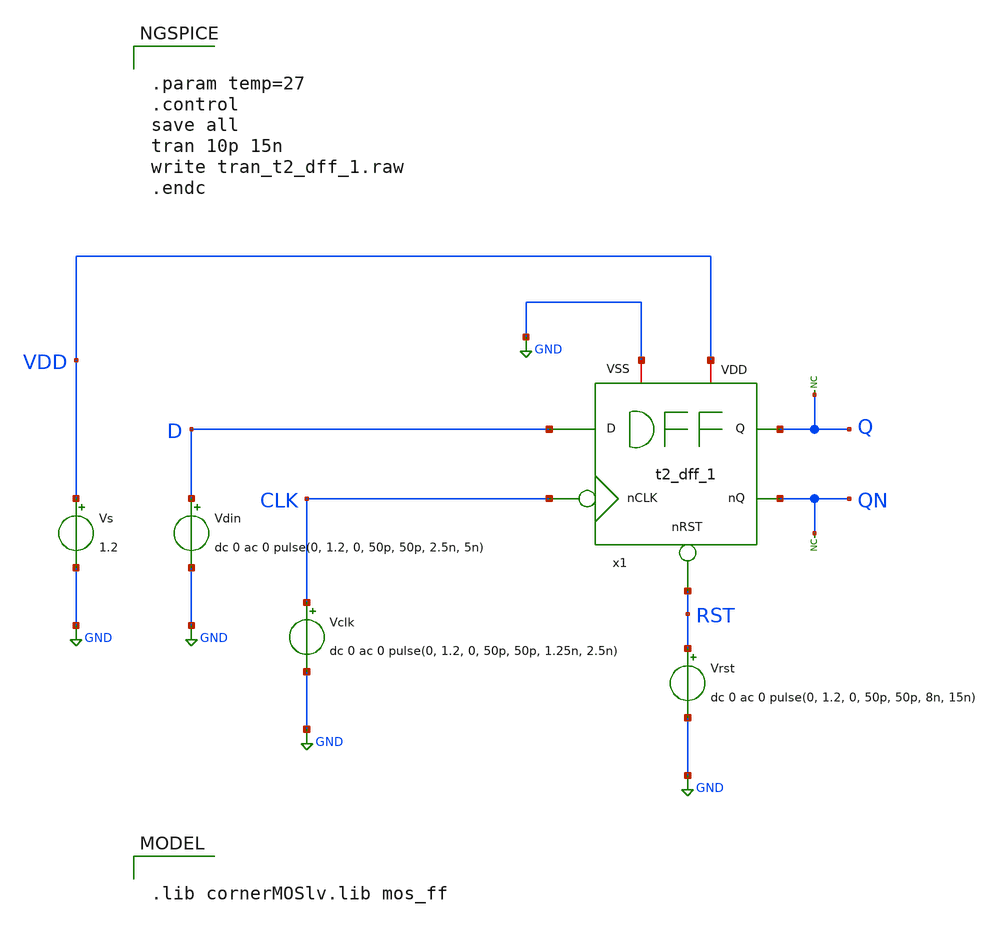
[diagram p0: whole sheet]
** sch_path: Team 2 Design/design_data/xschem/t2_dff_1_tb.sch
**.subckt t2_dff_1_tb
Vs VDD GND 1.2
* noconn Q
* noconn QN
Vdin D GND dc 0 ac 0 pulse(0, 1.2, 0, 50p, 50p, 2.5n, 5n)
Vclk CLK GND dc 0 ac 0 pulse(0, 1.2, 0, 50p, 50p, 1.25n, 2.5n)
Vrst RST GND dc 0 ac 0 pulse(0, 1.2, 0, 50p, 50p, 8n, 15n)
x1 VDD GND D CLK RST Q QN t2_dff_1
**** begin user architecture code


.param temp=27
.control
save all
tran 10p 15n
write tran_t2_dff_1.raw
.endc



.lib cornerMOSlv.lib mos_ff

**** end user architecture code
**.ends

* expanding   symbol:  t2_dff_1.sym # of pins=7
** sym_path: Team 2 Design/design_data/xschem/t2_dff_1.sym
** sch_path: Team 2 Design/design_data/xschem/t2_dff_1.sch
.subckt t2_dff_1 VDD VSS D CLK RST Q QN
*.iopin VSS
*.ipin D
*.ipin RST
*.opin Q
*.iopin VDD
*.opin QN
*.ipin CLK
x3 VDD net1 QN Q VSS t2_nand2
x4 VDD VSS Q net2 RST QN t2_nand3
x1 VDD VSS net4 net5 RST net1 t2_nand3
x2 VDD VSS net1 net5 net3 net2 t2_nand3
x6 VDD net3 net1 net4 VSS t2_nand2
x5 VDD VSS net2 D RST net3 t2_nand3
x7 VDD CLK net5 VSS t2_inverter
.ends


* expanding   symbol:  t2_nand2.sym # of pins=5
** sym_path: Team 2 Design/design_data/xschem/t2_nand2.sym
** sch_path: Team 2 Design/design_data/xschem/t2_nand2.sch
.subckt t2_nand2 VDD inA inB out VSS
*.iopin VSS
*.ipin inA
*.ipin inB
*.opin out
*.iopin VDD
XM1 out inA VDD VDD sg13_lv_pmos w=1u l=0.45u ng=1 m=1 mm_ok=1
XM2 out inB VDD VDD sg13_lv_pmos w=1u l=0.45u ng=1 m=1 mm_ok=1
XM3 out inB net1 VSS sg13_lv_nmos w=0.5u l=0.45u ng=1 m=1 mm_ok=1
XM4 net1 inA VSS VSS sg13_lv_nmos w=0.5u l=0.45u ng=1 m=1 mm_ok=1
.ends


* expanding   symbol:  t2_nand3.sym # of pins=6
** sym_path: Team 2 Design/design_data/xschem/t2_nand3.sym
** sch_path: Team 2 Design/design_data/xschem/t2_nand3.sch
.subckt t2_nand3 VDD VSS inA inB inC out
*.iopin VSS
*.ipin inA
*.ipin inC
*.opin out
*.iopin VDD
*.ipin inB
XM1 out inB VDD VDD sg13_lv_pmos w=0.3u l=0.15u ng=1 m=1 mm_ok=1
XM2 out inC VDD VDD sg13_lv_pmos w=0.3u l=0.13u ng=1 m=1 mm_ok=1
XM3 out inC net1 VSS sg13_lv_nmos w=0.15u l=0.13u ng=1 m=1 mm_ok=1
XM4 net1 inB net2 VSS sg13_lv_nmos w=0.15u l=0.13u ng=1 m=1 mm_ok=1
XM5 net2 inA VSS VSS sg13_lv_nmos w=0.15u l=0.13u ng=1 m=1 mm_ok=1
XM0 out inA VDD VDD sg13_lv_pmos w=0.3u l=0.15u ng=1 m=1 mm_ok=1
.ends


* expanding   symbol:  t2_inverter.sym # of pins=4
** sym_path: Team 2 Design/design_data/xschem/t2_inverter.sym
** sch_path: Team 2 Design/design_data/xschem/t2_inverter.sch
.subckt t2_inverter VP A Y VN
*.iopin VP
*.iopin VN
*.ipin A
*.opin Y
XM2 Y A VP VP sg13_lv_pmos w=0.3u l=0.13u ng=1 m=1 mm_ok=1
XM1 Y A VN VN sg13_lv_nmos w=0.15u l=0.13u ng=1 m=1 mm_ok=1
.ends

.GLOBAL GND
.end
